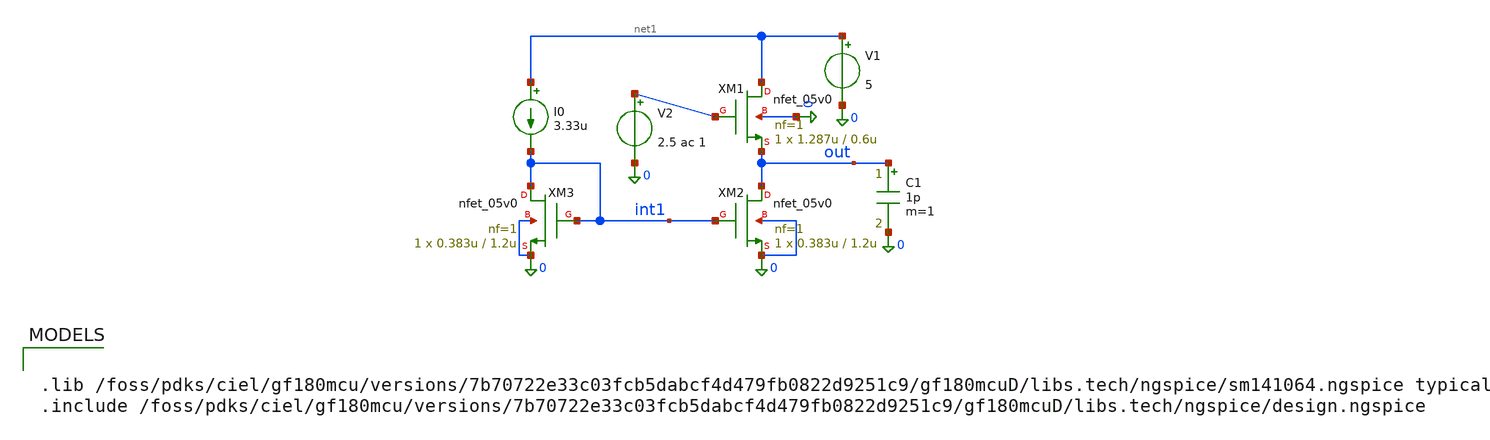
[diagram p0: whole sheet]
** sch_path: RN_buffer/buffer.sch
**.subckt buffer
XM1 net1 net2 out 0 nfet_05v0 L=0.6u W=1.287u nf=1 ad='int((nf+1)/2) * W/nf * 0.18u' as='int((nf+2)/2) * W/nf * 0.18u'
+ pd='2*int((nf+1)/2) * (W/nf + 0.18u)' ps='2*int((nf+2)/2) * (W/nf + 0.18u)' nrd='0.18u / W' nrs='0.18u / W'
+ sa=0 sb=0 sd=0 m=1
XM2 out int1 0 0 nfet_05v0 L=1.2u W=0.383u nf=1 ad='int((nf+1)/2) * W/nf * 0.18u' as='int((nf+2)/2) * W/nf * 0.18u'
+ pd='2*int((nf+1)/2) * (W/nf + 0.18u)' ps='2*int((nf+2)/2) * (W/nf + 0.18u)' nrd='0.18u / W' nrs='0.18u / W'
+ sa=0 sb=0 sd=0 m=1
V1 net1 0 5
V2 net2 0 2.5 ac 1
XM3 int1 int1 0 0 nfet_05v0 L=1.2u W=0.383u nf=1 ad='int((nf+1)/2) * W/nf * 0.18u' as='int((nf+2)/2) * W/nf * 0.18u'
+ pd='2*int((nf+1)/2) * (W/nf + 0.18u)' ps='2*int((nf+2)/2) * (W/nf + 0.18u)' nrd='0.18u / W' nrs='0.18u / W'
+ sa=0 sb=0 sd=0 m=1
I0 net1 int1 3.33u
C1 out 0 1p m=1
**** begin user architecture code


.control
  	save all
	op
	ac dec 20 1 100Meg
	remzerovec
	write buffer_op.raw
.endc

.options savecurrents




.lib /foss/pdks/ciel/gf180mcu/versions/7b70722e33c03fcb5dabcf4d479fb0822d9251c9/gf180mcuD/libs.tech/ngspice/sm141064.ngspice typical
.include /foss/pdks/ciel/gf180mcu/versions/7b70722e33c03fcb5dabcf4d479fb0822d9251c9/gf180mcuD/libs.tech/ngspice/design.ngspice


**** end user architecture code
**.ends
.end
